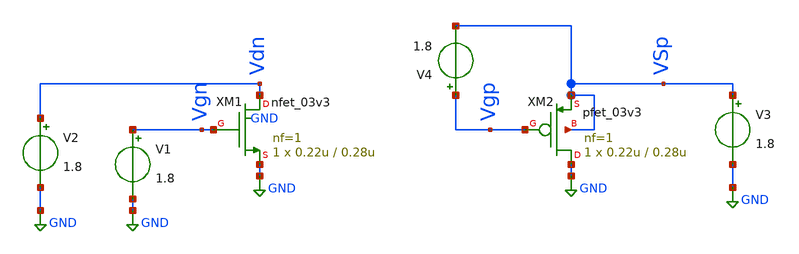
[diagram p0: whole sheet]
** sch_path: xschem/caracterizador/charac.sch
* Copyright 2022 GlobalFoundries PDK Authors
* Licensed under the Apache License, Version 2.0 (the "License");
* you may not use this file except in compliance with the License.
* You may obtain a copy of the License at
* https://www.apache.org/licenses/LICENSE-2.0
* Unless required by applicable law or agreed to in writing, software
* distributed under the License is distributed on an "AS IS" BASIS,
* WITHOUT WARRANTIES OR CONDITIONS OF ANY KIND, either express or implied.
* See the License for the specific language governing permissions and
* limitations under the License.
**.subckt charac
XM1 Vdn Vgn GND GND nfet_03v3 L=0.28u W=0.22u nf=1 ad='int((nf+1)/2) * W/nf * 0.18u' as='int((nf+2)/2) * W/nf * 0.18u'
+ pd='2*int((nf+1)/2) * (W/nf + 0.18u)' ps='2*int((nf+2)/2) * (W/nf + 0.18u)' nrd='0.18u / W' nrs='0.18u / W'
+ sa=0 sb=0 sd=0 m=1 par=1
XM2 GND Vgp VSp VSp pfet_03v3 L=0.28u W=0.22u nf=1 ad='int((nf+1)/2) * W/nf * 0.18u' as='int((nf+2)/2) * W/nf * 0.18u'
+ pd='2*int((nf+1)/2) * (W/nf + 0.18u)' ps='2*int((nf+2)/2) * (W/nf + 0.18u)' nrd='0.18u / W' nrs='0.18u / W'
+ sa=0 sb=0 sd=0 m=1 par=1
V1 Vgn GND 1.8
V2 Vdn GND 1.8
V3 VSp GND 1.8
V4 Vgp VSp 1.8
**** begin user architecture code



.control
  save all

* ======================= CONFIGURACIÓN PERSONALIZADA DE COLORES Y ESTILO ========================
set color0=white * Fondo blanco (o 'black' si prefieres fondo oscuro) [1, 2]
set color1=black * Texto y rejilla negros (si el fondo es blanco) [1, 2]
set color2=red * 1ª curva
set color3=blue * 2ª curva
set color4=green * 3ª curva
set color5=magenta * 4ª curva
set color6=cyan * 5ª curva
set color7=orange * 6ª curva
set color8=darkgreen * 7ª curva
set xbrushwidth=2 * Hace el trazo de las curvas más grueso y visible [2, 4]

  * ===== NMOS =====
  dc V2 0 3.3 0.01 V1 0 3.3 0.55
  plot -i(V2) title 'NMOS Output' xlabel 'VDS' ylabel 'ID'

  dc V1 0 3.3 0.01 V2 0.55 3.3 0.55
  plot -i(V2) title 'NMOS Transfer' xlabel 'VGS' ylabel 'ID'

  alter V2 = 1.65
  dc V1 0 3.3 0.01
  let idn = -i(V2)
  let gmn = deriv(idn)
  let gmidn = gmn/idn
  plot gmidn vs idn xlog xlimit 1e-9 1e-3 ylimit 0 35 title 'NMOS gm/Id' xlabel 'ID' ylabel 'gm/ID (1/V)'

  * ===== PMOS (V3 = VSD, V4 = VGS negativo, referido a la fuente) =====
  dc V3 0 3.3 0.01 V4 0 -3.3 -0.55
  plot -i(V3) title 'PMOS Output' xlabel 'VSD' ylabel '|ID|'

  dc V4 0 -3.3 -0.01 V3 0.55 3.3 0.55
  plot -i(V3) title 'PMOS Transfer' xlabel 'VGS' ylabel '|ID|'

  alter V3 = 1.65
  dc V4 0 -3.3 -0.01
  let idp = -i(V3)
  let gmp = abs(deriv(idp))
  let gmidp = gmp/idp
  plot gmidp vs idp xlog xlimit 1e-9 1e-3 ylimit 0 35 title 'PMOS gm/Id' xlabel '|ID| (A)' ylabel 'gm/ID (1/V)'
.endc




.include /home/ringosinye/eda/pdks/gf180mcuD/libs.tech/ngspice/design.ngspice
.lib /home/ringosinye/eda/pdks/gf180mcuD/libs.tech/ngspice/sm141064.ngspice typical
.param sw_stat_mismatch = 0




.control
save all

* Coloracion de graficas
set color0=white
set color1=black
set color2=blue
set xbrushwidth=2

* ========================================================
* 1. CARACTERIZACION NMOS (Voltaje fijo VDS = 1.65 V)
* ========================================================
alter V2 = 1.65
dc V1 0 3.3 0.01

let idn = abs(-i(V2)) + 1e-15
let gmn = deriv(idn)
let gmidn = gmn/idn

* --- MEDICIONES AUTOMATICAS NMOS ---
meas dc vth_n find v(vgn) when idn=100n
meas dc gmn_max max gmn
meas dc id_inv_mod_n find idn when gmidn=15

* Guardar valores numéricos en variables antes de cambiar de simulación
set vth_val = $&vth_n
set gmn_val = $&gmn_max
set id_mod_val = $&id_inv_mod_n

* ========================================================
* 2. RESISTENCIA DE SALIDA NMOS (ro) en VGS = 1.65 V
* ========================================================
alter V1 = 1.65
dc V2 0 3.3 0.01

let idn_sat = abs(-i(V2))
let gds_vec = deriv(idn_sat)
meas dc gds_n find gds_vec at=1.65

set gds_val = $&gds_n
let ro_n = 1 / gds_n
let av_n = $gmn_val * ro_n

set ro_val = $&ro_n
set av_val = $&av_n

* --- IMPRIMIR RESULTADOS EN CONSOLA ---
echo ================ RESUMEN NMOS ================
echo Vth_n = $vth_val V
echo gmn_max = $gmn_val S
echo ID_inv_mod_n = $id_mod_val A
echo gds_n = $gds_val S
echo ro_n = $ro_val Ohms
echo Av_n (gm*ro) = $av_val V/V
echo ==============================================
.endc


**** end user architecture code
**.ends
.GLOBAL GND
.end
